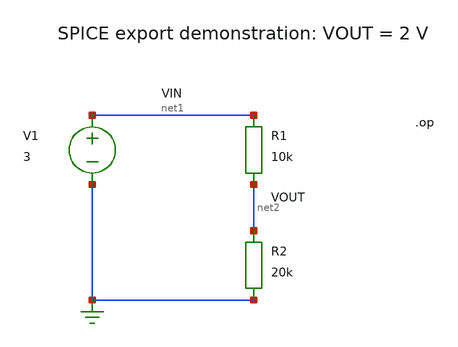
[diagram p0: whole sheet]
** sch_path: examples/spice.sch
**.subckt spice
R1 net1 net2 10k
R2 net2 0 20k
V1 net1 0 3
**** begin user architecture code
.op
**** end user architecture code
**.ends
.end
